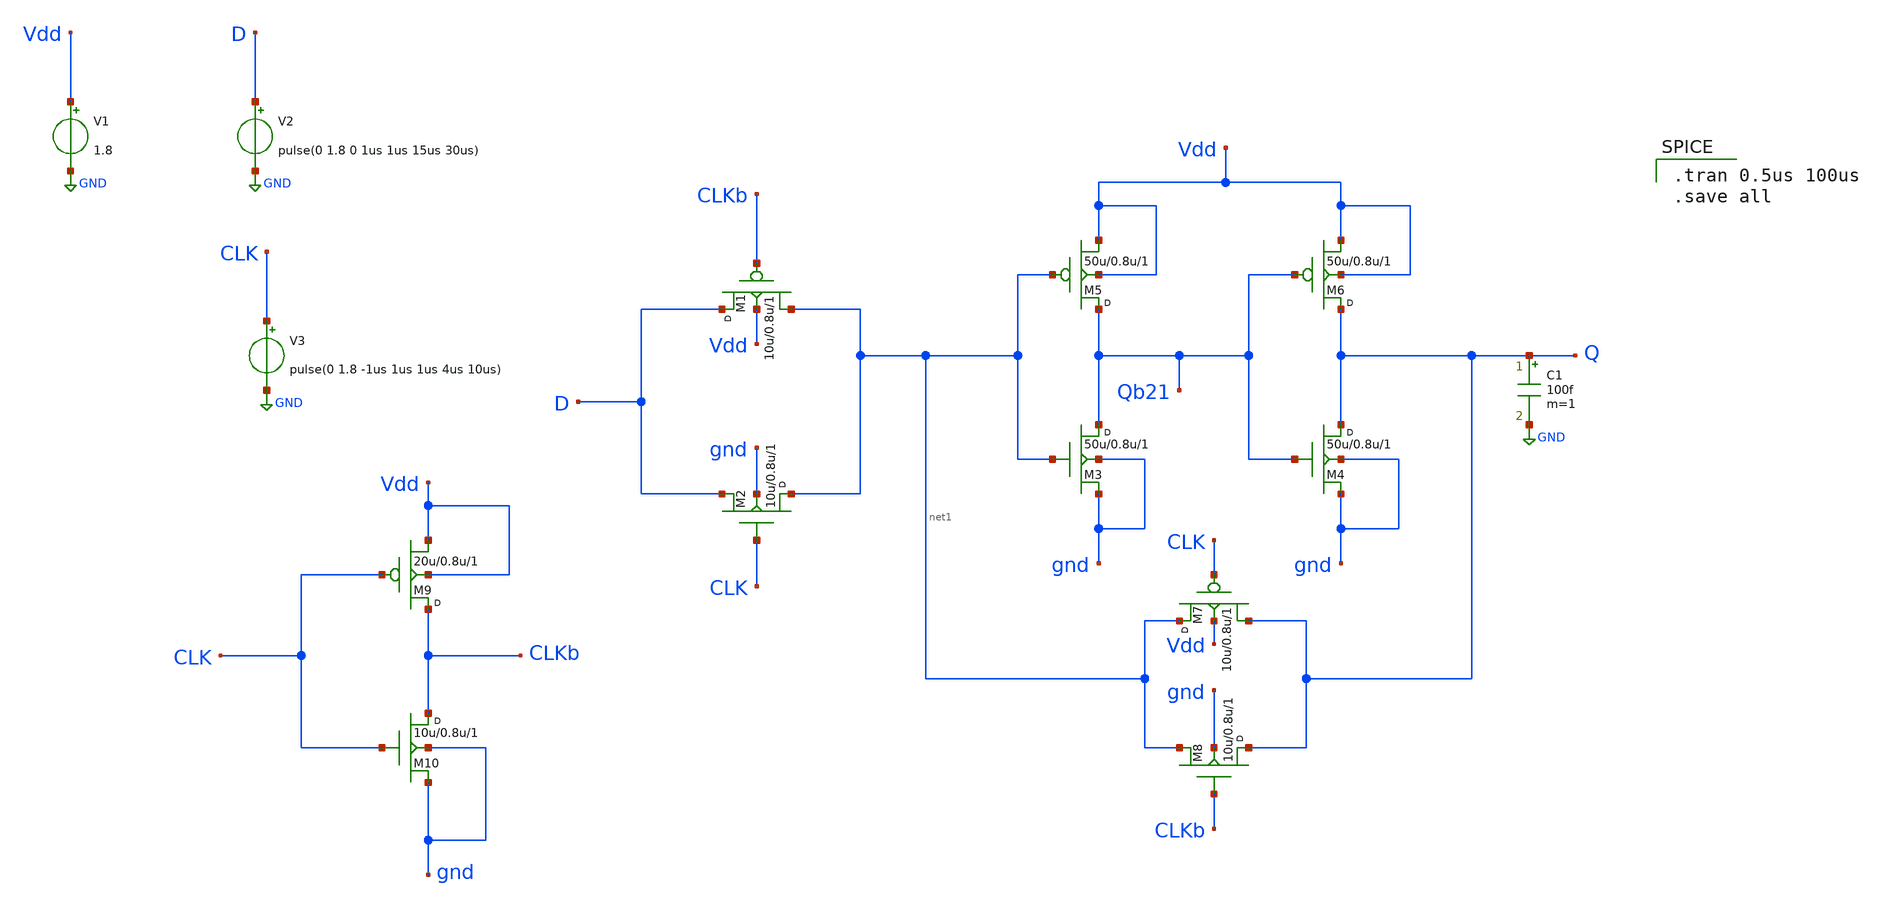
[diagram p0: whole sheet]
** sch_path: cells/dffq/DFlip-flop3.sch
**.subckt DFlip-flop3
M1 D CLKb net1 Vdd p1 w=10u l=0.8u m=1
M2 net1 CLK D gnd n1 w=10u l=0.8u m=1
M3 Qb21 net1 gnd gnd n1 w=50u l=0.8u m=1
M4 Q Qb21 gnd gnd n1 w=50u l=0.8u m=1
M5 Qb21 net1 Vdd Vdd p1 w=50u l=0.8u m=1
M6 Q Qb21 Vdd Vdd p1 w=50u l=0.8u m=1
M7 net1 CLK Q Vdd p1 w=10u l=0.8u m=1
M8 Q CLKb net1 gnd n1 w=10u l=0.8u m=1
M9 CLKb CLK Vdd Vdd p1 w=20u l=0.8u m=1
M10 CLKb CLK gnd gnd n1 w=10u l=0.8u m=1
V1 Vdd GND 1.8
V2 D GND pulse(0 1.8 0 1us 1us 15us 30us)
V3 CLK GND pulse(0 1.8 -1us 1us 1us 4us 10us)
C1 Q GND 100f m=1
**** begin user architecture code


.model n1 nmos level=49 version=3.3.0
.model p1 pmos level=49 version=3.3.0
.model n2 nmos level=2 version=3.3.0
.model p2 pmos level=2 version=3.3.0


.tran 0.5us 100us
.save all

**** end user architecture code
**.ends
.GLOBAL GND
.end
